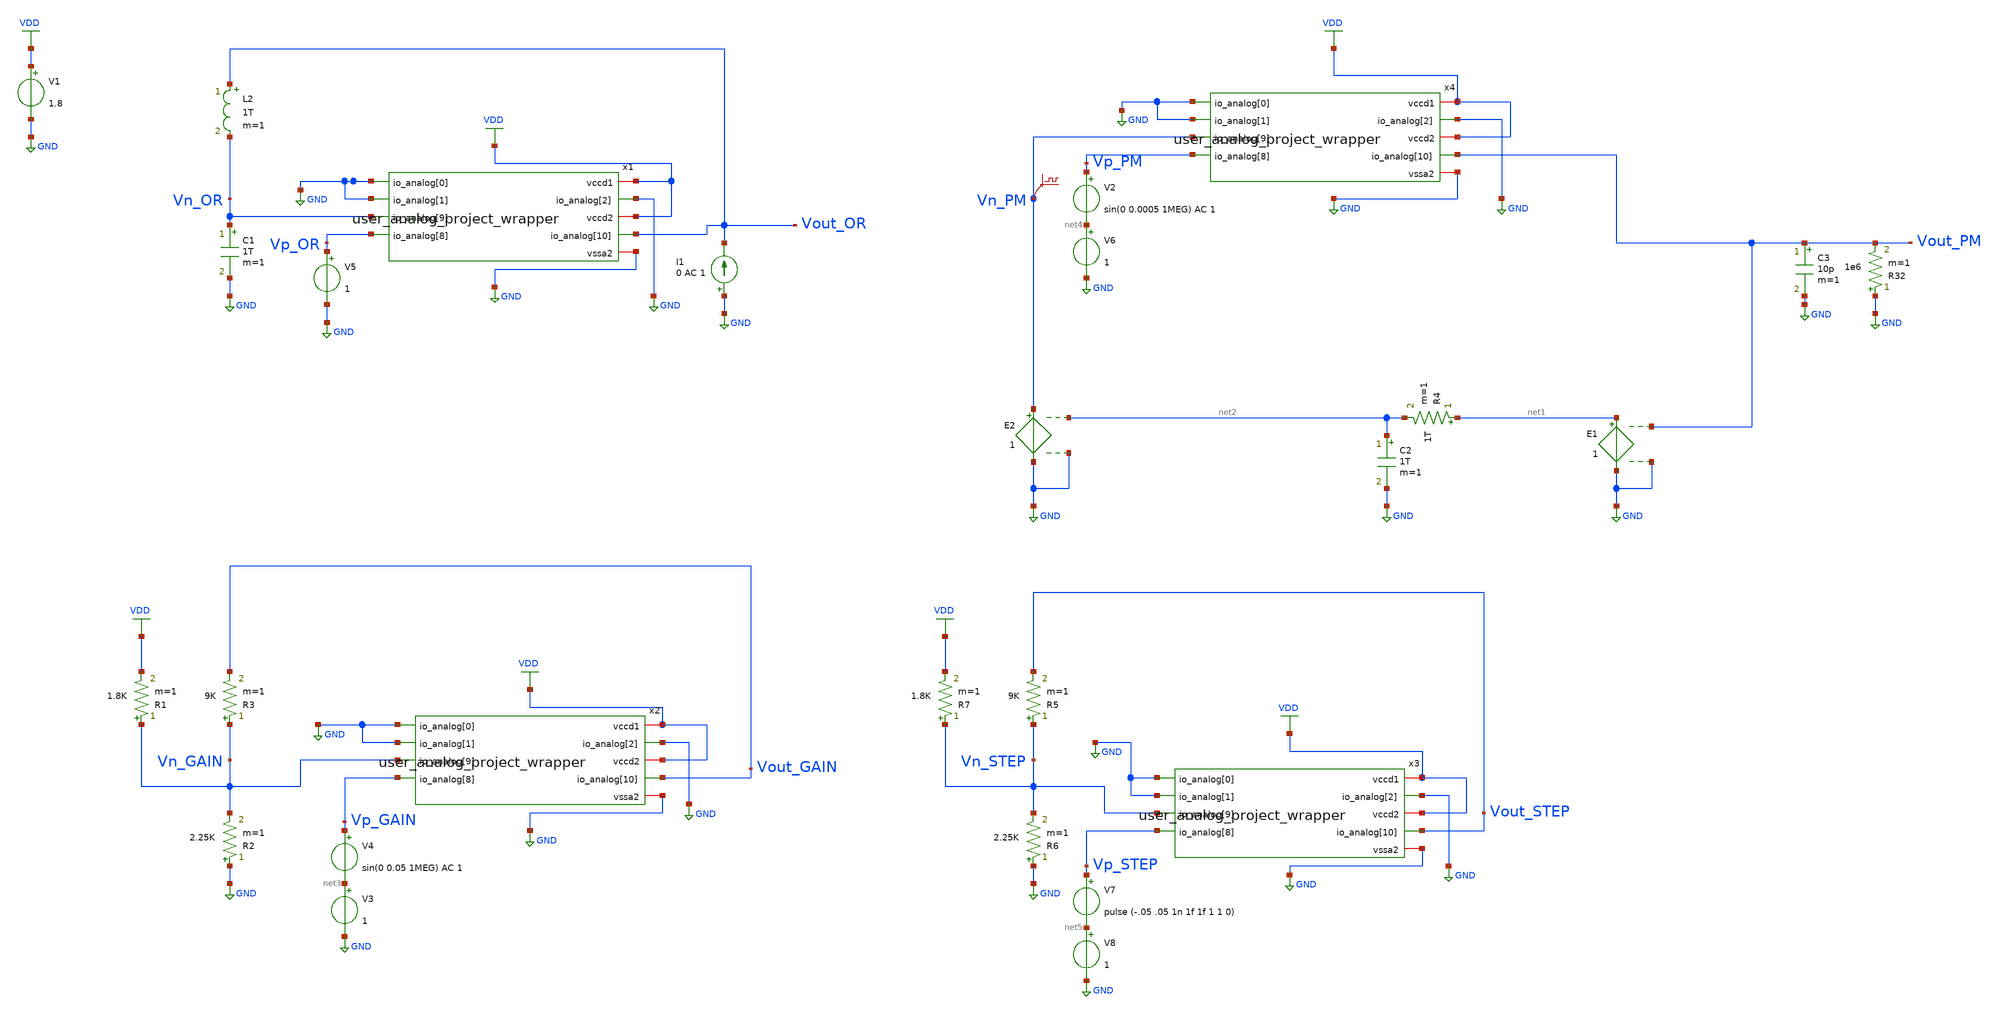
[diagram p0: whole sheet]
** sch_path: SP23_Tapeout/Tapeout_Ready_v5/OTA_GM_Schematic/ota_no_mirror_testing_031823_symbol.sch
**.subckt ota_no_mirror_testing_031823_symbol
V1 VDD GND 1.8
V5 Vp_OR GND 1
I1 GND Vout_OR 0 AC 1
L2 Vout_OR Vn_OR 1T m=1
C1 Vn_OR GND 1T m=1
R3 Vn_GAIN Vout_GAIN 9K m=1
R2 GND Vn_GAIN 2.25K m=1
R1 Vn_GAIN VDD 1.8K m=1
V4 Vp_GAIN net3 sin(0 0.05 1MEG) AC 1
V3 net3 GND 1
E1 net1 GND Vout_PM GND 1
E2 Vn_PM GND net2 GND 1
V6 net4 GND 1
V2 Vp_PM net4 sin(0 0.0005 1MEG) AC 1
C2 net2 GND 1T m=1
R4 net1 net2 1T m=1
.save v(vn_pm)
R5 Vn_STEP Vout_STEP 9K m=1
R6 GND Vn_STEP 2.25K m=1
R7 Vn_STEP VDD 1.8K m=1
V8 net5 GND 1
V7 Vp_STEP net5 pulse (-.05 .05 1n 1f 1f 1 1 0)
C3 Vout_PM GND 10p m=1
R32 GND Vout_PM 1e6 m=1
x1 GND Vout_OR GND GND Vp_OR Vn_OR GND VDD VDD user_analog_project_wrapper
x2 GND Vout_GAIN GND GND Vp_GAIN Vn_GAIN GND VDD VDD user_analog_project_wrapper
x3 GND Vout_STEP GND GND Vp_STEP Vn_STEP GND VDD VDD user_analog_project_wrapper
x4 GND Vout_PM GND GND Vp_PM Vn_PM GND VDD VDD user_analog_project_wrapper
**** begin user architecture code


.lib /foss/pdk/sky130A/libs.tech/ngspice/sky130.lib.spice tt
.include /foss/designs/Tapeout_Ready_v4/OTA_GM_Layout/user_analog_project_wrapper.spice

.control
save all


%tran 0.001u 5u
%op
ac dec 100 1K 5G
plot db(v(Vout_PM)) cph(v(Vout_PM))*180/pi
plot db(v(Vout_OR)) cph(v(Vout_PM))*180/pi
%plot v(Vout_GAIN)
%plot v(Vout_STEP)

write ota_no_mirror_testing_031823_symbol.raw
.endc


**** end user architecture code
**.ends
.GLOBAL VDD
.GLOBAL GND
.end
